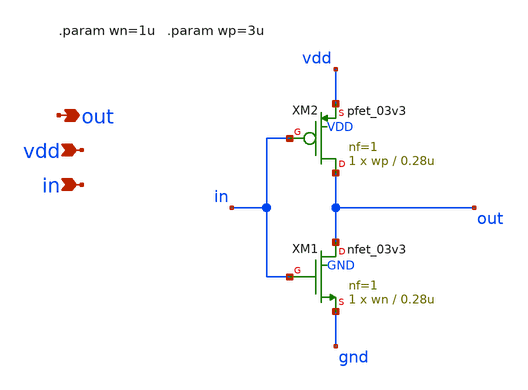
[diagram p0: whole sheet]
** sch_path: schematic pt2/xschem/inv.sch
**.subckt inv out vdd in
*.opin out
*.ipin vdd
*.ipin in
XM1 out in gnd GND nfet_03v3 L=0.28u W=wn nf=1 ad='int((nf+1)/2) * W/nf * 0.18u' as='int((nf+2)/2) * W/nf * 0.18u'
+ pd='2*int((nf+1)/2) * (W/nf + 0.18u)' ps='2*int((nf+2)/2) * (W/nf + 0.18u)' nrd='0.18u / W' nrs='0.18u / W'
+ sa=0 sb=0 sd=0 m=1 par=1
XM2 out in vdd VDD pfet_03v3 L=0.28u W=wp nf=1 ad='int((nf+1)/2) * W/nf * 0.18u' as='int((nf+2)/2) * W/nf * 0.18u'
+ pd='2*int((nf+1)/2) * (W/nf + 0.18u)' ps='2*int((nf+2)/2) * (W/nf + 0.18u)' nrd='0.18u / W' nrs='0.18u / W'
+ sa=0 sb=0 sd=0 m=1 par=1
**.ends
.end
